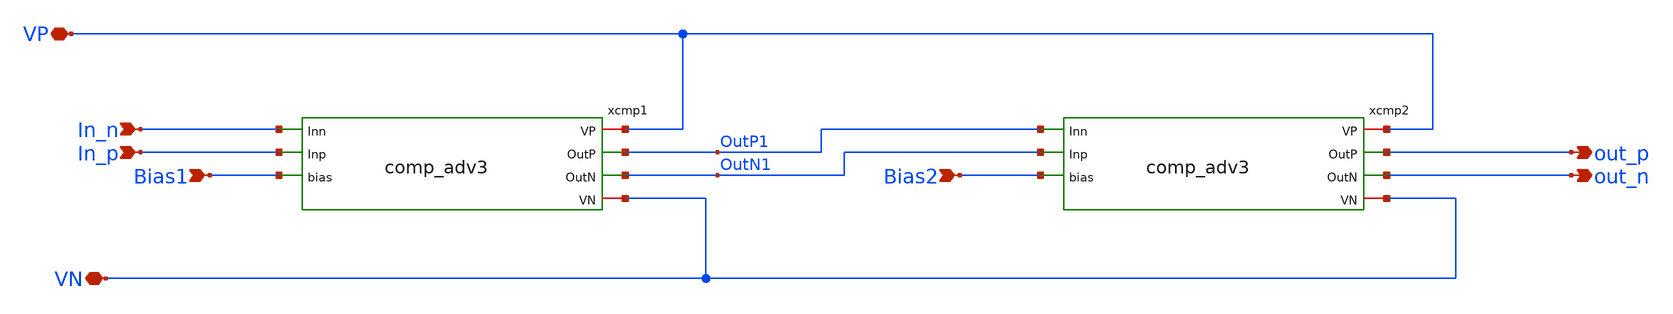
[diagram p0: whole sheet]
** sch_path: xschem/comp/comp_amp_20db_no_cmm.sch
**.subckt comp_amp_20db_no_cmm In_n In_p VP out_p out_n Bias1 Bias2 VN
*.ipin In_n
*.ipin In_p
*.iopin VP
*.opin out_p
*.opin out_n
*.ipin Bias1
*.ipin Bias2
*.iopin VN
xcmp2 VP out_p out_n OutP1 OutN1 Bias2 VN comp_adv3
xcmp1 VP OutP1 OutN1 In_n In_p Bias1 VN comp_adv3
**.ends

* expanding   symbol:  comp/comp_adv3.sym # of pins=7
** sym_path: xschem/comp/comp_adv3.sym
** sch_path: xschem/comp/comp_adv3.sch
.subckt comp_adv3 VP OutP OutN Inn Inp bias VN
*.ipin Inp
*.ipin bias
*.ipin Inn
*.iopin VP
*.iopin VN
*.opin OutN
*.opin OutP
XM1 OutN Inp VIq VN sky130_fd_pr__nfet_01v8_lvt L=0.15 W=2 nf=1 ad='int((nf+1)/2) * W/nf * 0.29' as='int((nf+2)/2) * W/nf * 0.29'
+ pd='2*int((nf+1)/2) * (W/nf + 0.29)' ps='2*int((nf+2)/2) * (W/nf + 0.29)' nrd='0.29 / W' nrs='0.29 / W'
+ sa=0 sb=0 sd=0 mult=6 m=6
XM2 OutP Inn VIq VN sky130_fd_pr__nfet_01v8_lvt L=0.15 W=2 nf=1 ad='int((nf+1)/2) * W/nf * 0.29' as='int((nf+2)/2) * W/nf * 0.29'
+ pd='2*int((nf+1)/2) * (W/nf + 0.29)' ps='2*int((nf+2)/2) * (W/nf + 0.29)' nrd='0.29 / W' nrs='0.29 / W'
+ sa=0 sb=0 sd=0 mult=6 m=6
XM7 bias bias VN VN sky130_fd_pr__nfet_01v8_lvt L=0.3 W=2 nf=1 ad='int((nf+1)/2) * W/nf * 0.29' as='int((nf+2)/2) * W/nf * 0.29'
+ pd='2*int((nf+1)/2) * (W/nf + 0.29)' ps='2*int((nf+2)/2) * (W/nf + 0.29)' nrd='0.29 / W' nrs='0.29 / W'
+ sa=0 sb=0 sd=0 mult=1 m=1
XM9 VIq bias VN VN sky130_fd_pr__nfet_01v8_lvt L=0.3 W=2 nf=1 ad='int((nf+1)/2) * W/nf * 0.29' as='int((nf+2)/2) * W/nf * 0.29'
+ pd='2*int((nf+1)/2) * (W/nf + 0.29)' ps='2*int((nf+2)/2) * (W/nf + 0.29)' nrd='0.29 / W' nrs='0.29 / W'
+ sa=0 sb=0 sd=0 mult=10 m=10
XR1 OutN VP VN sky130_fd_pr__res_xhigh_po_2p85 L=1.5 mult=1 m=1
XR2 OutP VP VN sky130_fd_pr__res_xhigh_po_2p85 L=1.5 mult=1 m=1
XM3 bias VN VN VN sky130_fd_pr__nfet_01v8_lvt L=0.3 W=2 nf=1 ad='int((nf+1)/2) * W/nf * 0.29' as='int((nf+2)/2) * W/nf * 0.29'
+ pd='2*int((nf+1)/2) * (W/nf + 0.29)' ps='2*int((nf+2)/2) * (W/nf + 0.29)' nrd='0.29 / W' nrs='0.29 / W'
+ sa=0 sb=0 sd=0 mult=1 m=1
.ends

.end
